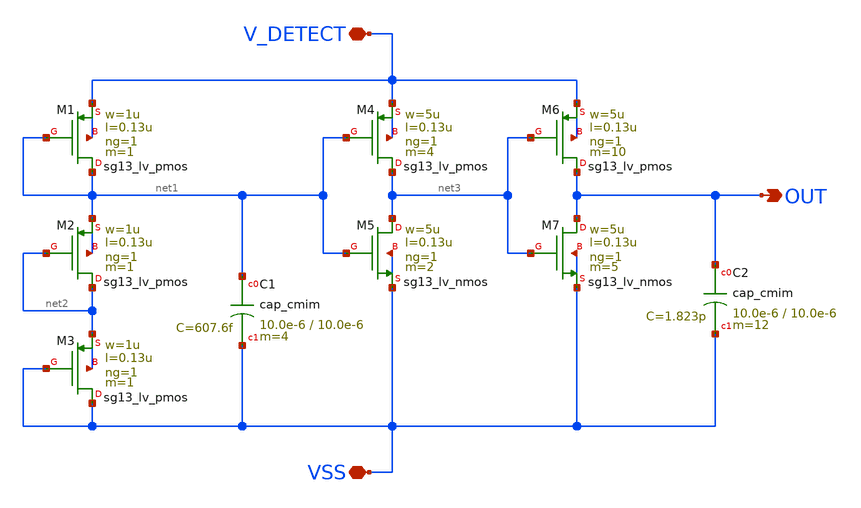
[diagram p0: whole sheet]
** sch_path: SSDOR_1.2V_v2/components/startup_ckt/startup_ckt.sch
**.subckt startup_ckt V_DETECT VSS OUT
*.iopin V_DETECT
*.iopin VSS
*.opin OUT
XM1 net1 net1 V_DETECT V_DETECT sg13_lv_pmos w=1u l=0.13u ng=1 m=1 mm_ok=1
XM2 net2 net2 net1 net1 sg13_lv_pmos w=1u l=0.13u ng=1 m=1 mm_ok=1
XM3 VSS VSS net2 net2 sg13_lv_pmos w=1u l=0.13u ng=1 m=1 mm_ok=1
XM4 net3 net1 V_DETECT V_DETECT sg13_lv_pmos w=5u l=0.13u ng=1 m=4 mm_ok=1
XM5 net3 net1 VSS VSS sg13_lv_nmos w=5u l=0.13u ng=1 m=2 mm_ok=1
XM6 OUT net3 V_DETECT V_DETECT sg13_lv_pmos w=5u l=0.13u ng=1 m=10 mm_ok=1
XM7 OUT net3 VSS VSS sg13_lv_nmos w=5u l=0.13u ng=1 m=5 mm_ok=1
XC1 net1 VSS cap_cmim w=10.0e-6 l=10.0e-6 m=4 mm_ok=1
XC2 OUT VSS cap_cmim w=10.0e-6 l=10.0e-6 m=12 mm_ok=1
**.ends
.end
